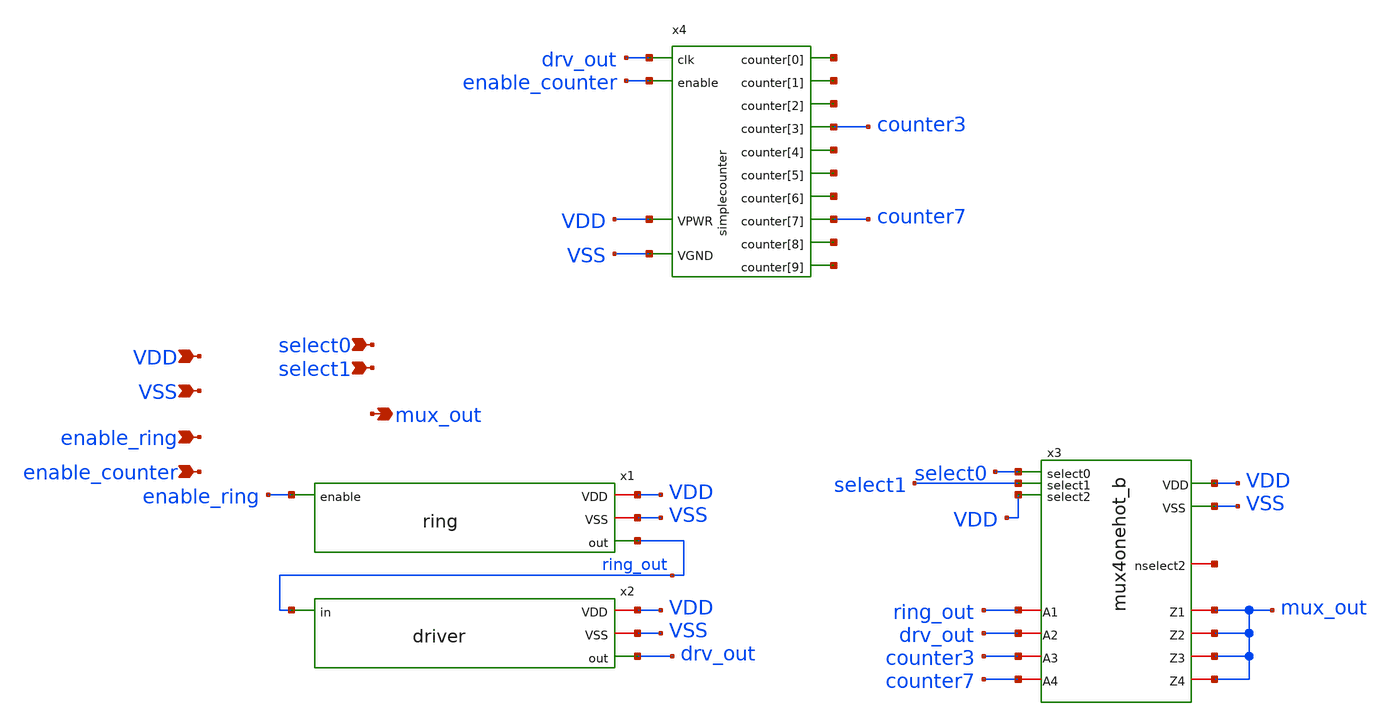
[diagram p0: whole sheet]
** sch_path: xschem/ringtest.sch
**.subckt ringtest VDD VSS enable_ring select0 select1 enable_counter mux_out
*.ipin VDD
*.ipin VSS
*.ipin enable_ring
*.ipin select0
*.ipin select1
*.ipin enable_counter
*.opin mux_out
x3 select1 VDD VSS counter3 drv_out ring_out mux_out mux_out mux_out counter7 mux_out select0 VDD
+ net1 mux4onehot_b
x4 VSS VDD drv_out enable_counter net2 net3 net4 counter3 net5 net6 net7 counter7 net8 net9
+ simplecounter
x1 VDD VSS enable_ring ring_out ring
x2 VDD VSS ring_out drv_out driver
**.ends
.end
